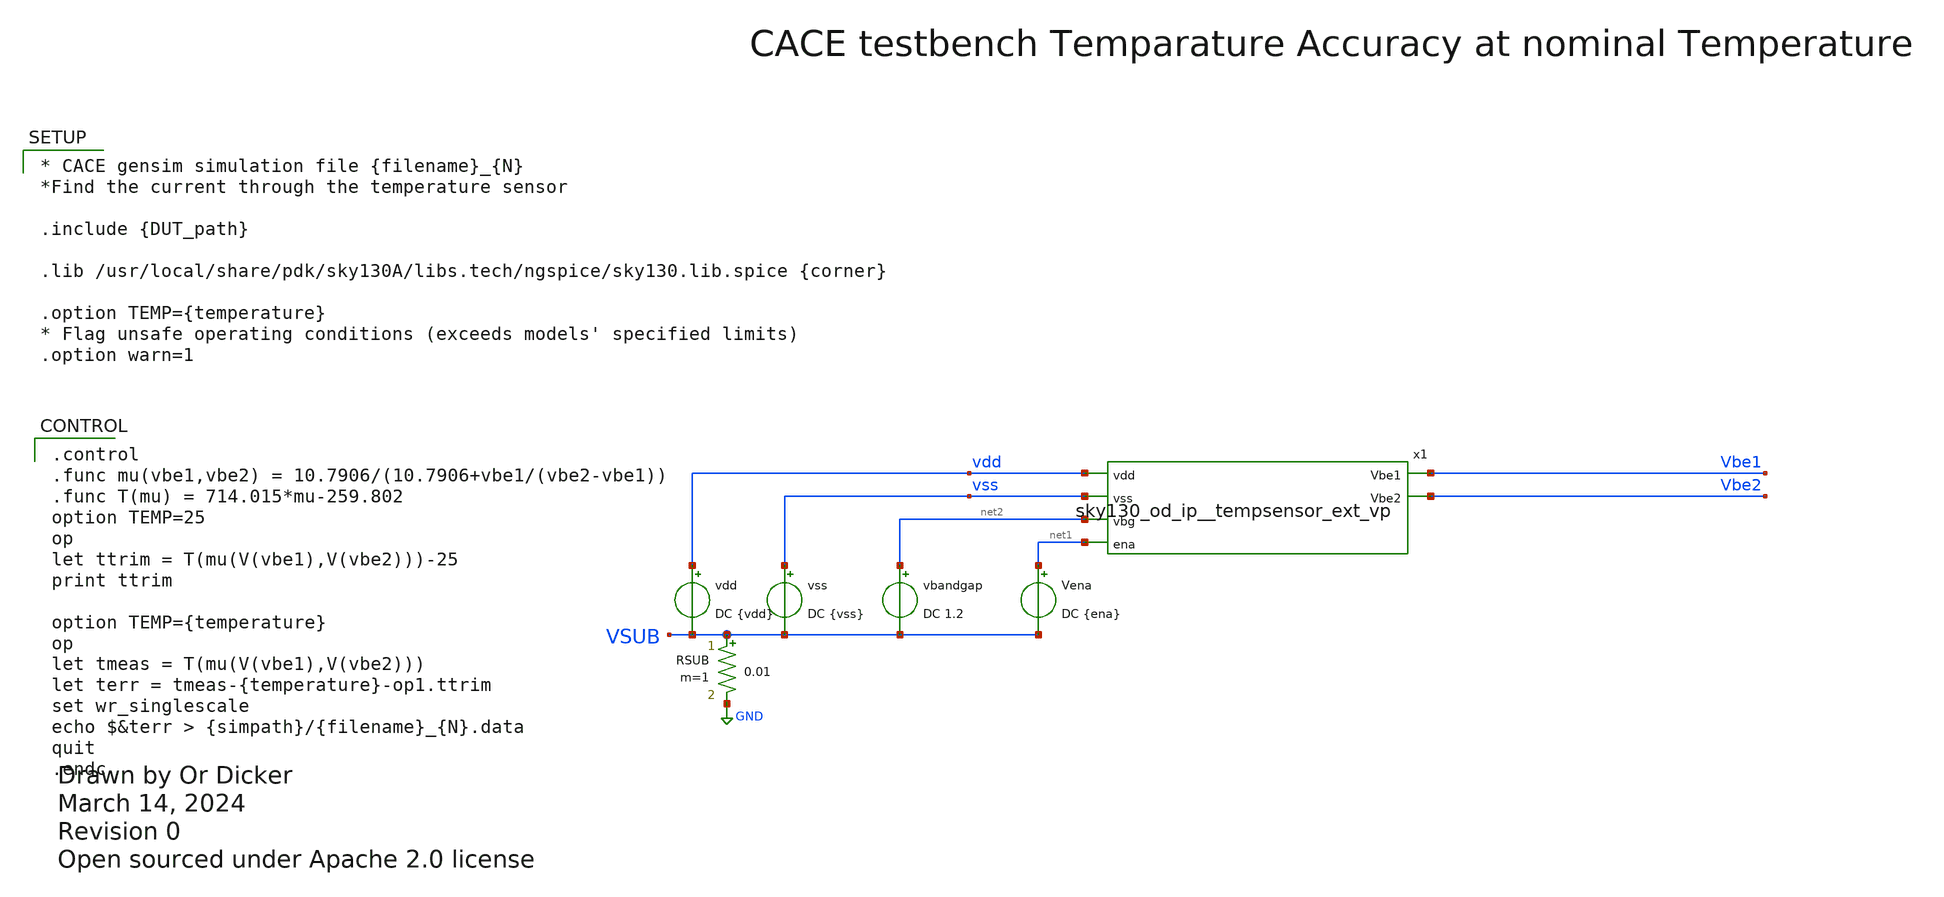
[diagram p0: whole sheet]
** sch_path: cace/temperature.sch
* Open sourced under Apache 2.0 license
**.subckt temperature
vss vss VSUB DC {vss}
vdd vdd VSUB DC {vdd}
RSUB VSUB GND 0.01 m=1
Vena net1 VSUB DC {ena}
x1 vdd vss net2 Vbe1 Vbe2 net1 sky130_od_ip__tempsensor_ext_vp
vbandgap net2 VSUB DC 1.2
**** begin user architecture code

.control
.func mu(vbe1,vbe2) = 10.7906/(10.7906+vbe1/(vbe2-vbe1))
.func T(mu) = 714.015*mu-259.802
option TEMP=25
op
let ttrim = T(mu(V(vbe1),V(vbe2)))-25
print ttrim

option TEMP={temperature}
op
let tmeas = T(mu(V(vbe1),V(vbe2)))
let terr = tmeas-{temperature}-op1.ttrim
set wr_singlescale
echo $&terr > {simpath}/{filename}_{N}.data
quit
.endc



* CACE gensim simulation file {filename}_{N}
*Find the current through the temperature sensor

.include {DUT_path}

.lib /usr/local/share/pdk/sky130A/libs.tech/ngspice/sky130.lib.spice {corner}

.option TEMP={temperature}
* Flag unsafe operating conditions (exceeds models' specified limits)
.option warn=1


**** end user architecture code
**.ends

* expanding   symbol:  xschem/sky130_od_ip__tempsensor_ext_vp.sym # of pins=6
** sym_path: xschem/sky130_od_ip__tempsensor_ext_vp.sym
** sch_path: xschem/sky130_od_ip__tempsensor_ext_vp.sch
.subckt sky130_od_ip__tempsensor_ext_vp vdd vss vbg Vbe1 Vbe2 ena
*.ipin vdd
*.ipin vss
*.opin Vbe2
*.opin Vbe1
*.ipin ena
*.ipin vbg
XQ_BL1 vss vss Vbe1 sky130_fd_pr__pnp_05v5_W3p40L3p40 m=1
XQ_BR1 vss vss Vbe2 sky130_fd_pr__pnp_05v5_W3p40L3p40 m=1
XM1 Vbe1 vp vdd VDD sky130_fd_pr__pfet_01v8_lvt L=1 W=1 nf=1 ad='int((nf+1)/2) * W/nf * 0.29' as='int((nf+2)/2)
+ * W/nf * 0.29' pd='2*int((nf+1)/2) * (W/nf + 0.29)' ps='2*int((nf+2)/2) * (W/nf + 0.29)' nrd='0.29 /
+ W' nrs='0.29 / W' sa=0 sb=0 sd=0 mult=1 m=1
XM2 Vbe2 vp vdd VDD sky130_fd_pr__pfet_01v8_lvt L=1 W=1 nf=1 ad='int((nf+1)/2) * W/nf * 0.29' as='int((nf+2)/2)
+ * W/nf * 0.29' pd='2*int((nf+1)/2) * (W/nf + 0.29)' ps='2*int((nf+2)/2) * (W/nf + 0.29)' nrd='0.29 /
+ W' nrs='0.29 / W' sa=0 sb=0 sd=0 mult=5 m=5
XM4 net2 vbg net1 vss sky130_fd_pr__nfet_01v8 L=1 W=1 nf=1 ad='int((nf+1)/2) * W/nf * 0.29' as='int((nf+2)/2)
+ * W/nf * 0.29' pd='2*int((nf+1)/2) * (W/nf + 0.29)' ps='2*int((nf+2)/2) * (W/nf + 0.29)' nrd='0.29 /
+ W' nrs='0.29 / W' sa=0 sb=0 sd=0 mult=1 m=1
XM5 vp vp net1 vss sky130_fd_pr__nfet_01v8 L=1 W=1 nf=1 ad='int((nf+1)/2) * W/nf * 0.29' as='int((nf+2)/2)
+ * W/nf * 0.29' pd='2*int((nf+1)/2) * (W/nf + 0.29)' ps='2*int((nf+2)/2) * (W/nf + 0.29)' nrd='0.29 /
+ W' nrs='0.29 / W' sa=0 sb=0 sd=0 mult=1 m=1
XM7 vp net2 vdd vdd sky130_fd_pr__pfet_01v8 L=1 W=10 nf=1 ad='int((nf+1)/2) * W/nf * 0.29' as='int((nf+2)/2)
+ * W/nf * 0.29' pd='2*int((nf+1)/2) * (W/nf + 0.29)' ps='2*int((nf+2)/2) * (W/nf + 0.29)' nrd='0.29 /
+ W' nrs='0.29 / W' sa=0 sb=0 sd=0 mult=1 m=1
XM8 net2 net2 vdd vdd sky130_fd_pr__pfet_01v8 L=1 W=10 nf=1 ad='int((nf+1)/2) * W/nf * 0.29' as='int((nf+2)/2)
+ * W/nf * 0.29' pd='2*int((nf+1)/2) * (W/nf + 0.29)' ps='2*int((nf+2)/2) * (W/nf + 0.29)' nrd='0.29 /
+ W' nrs='0.29 / W' sa=0 sb=0 sd=0 mult=1 m=1
XM3 vp ena vdd vdd sky130_fd_pr__pfet_01v8 L=1 W=1 nf=1 ad='int((nf+1)/2) * W/nf * 0.29' as='int((nf+2)/2)
+ * W/nf * 0.29' pd='2*int((nf+1)/2) * (W/nf + 0.29)' ps='2*int((nf+2)/2) * (W/nf + 0.29)' nrd='0.29 /
+ W' nrs='0.29 / W' sa=0 sb=0 sd=0 mult=1 m=1
XM6 net1 ena vss vss sky130_fd_pr__nfet_01v8 L=20 W=1 nf=1 ad='int((nf+1)/2) * W/nf * 0.29' as='int((nf+2)/2)
+ * W/nf * 0.29' pd='2*int((nf+1)/2) * (W/nf + 0.29)' ps='2*int((nf+2)/2) * (W/nf + 0.29)' nrd='0.29 /
+ W' nrs='0.29 / W' sa=0 sb=0 sd=0 mult=1 m=1
.ends

.GLOBAL GND
.end
